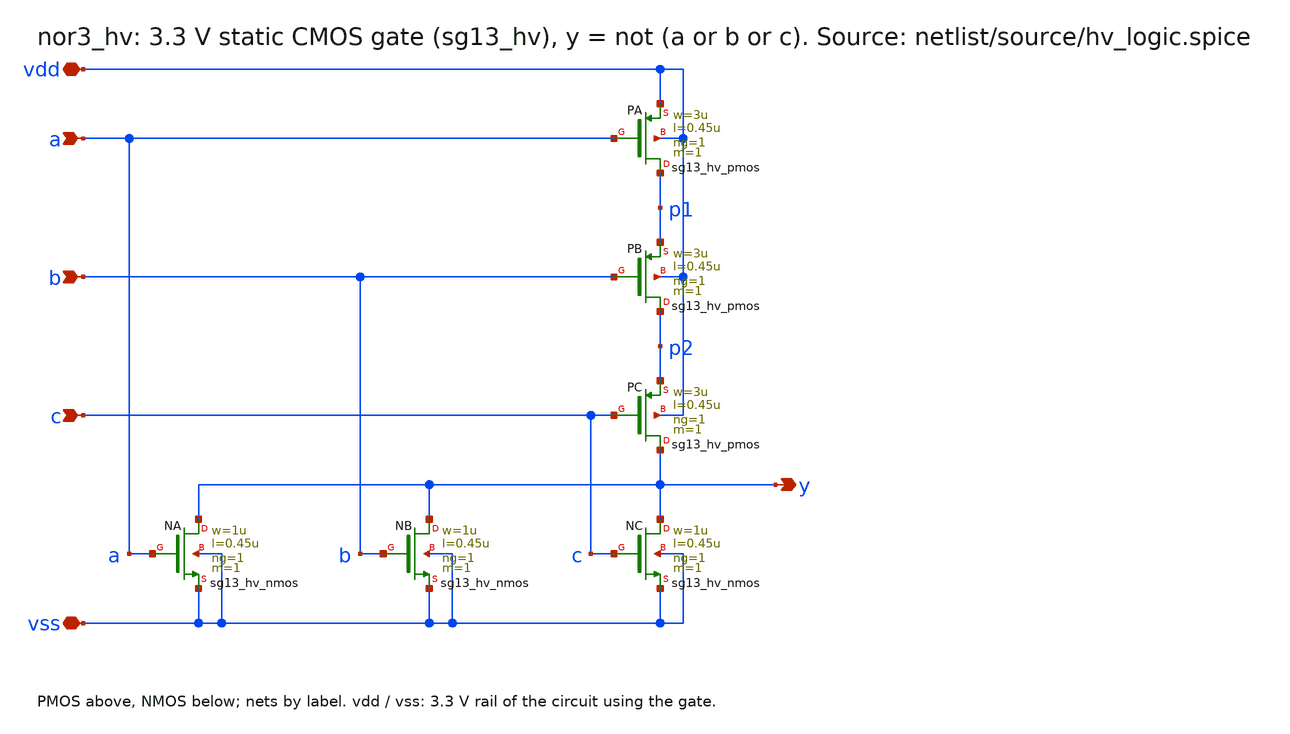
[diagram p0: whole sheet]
** sch_path: sudelbuecher/design_considerations/consolidation/bias_hierarchy_2026-10-27/before/macros/hv_logic/schematic/xschem/nor3_hv.sch
**.subckt nor3_hv vdd vss a b c y
*.iopin vdd
*.iopin vss
*.ipin a
*.ipin b
*.ipin c
*.opin y
XPA p1 a vdd vdd sg13_hv_pmos w=3u l=0.45u ng=1 m=1 mm_ok=1
XPB p2 b p1 vdd sg13_hv_pmos w=3u l=0.45u ng=1 m=1 mm_ok=1
XPC y c p2 vdd sg13_hv_pmos w=3u l=0.45u ng=1 m=1 mm_ok=1
XNA y a vss vss sg13_hv_nmos w=1u l=0.45u ng=1 m=1 mm_ok=1
XNB y b vss vss sg13_hv_nmos w=1u l=0.45u ng=1 m=1 mm_ok=1
XNC y c vss vss sg13_hv_nmos w=1u l=0.45u ng=1 m=1 mm_ok=1
**.ends
.end
